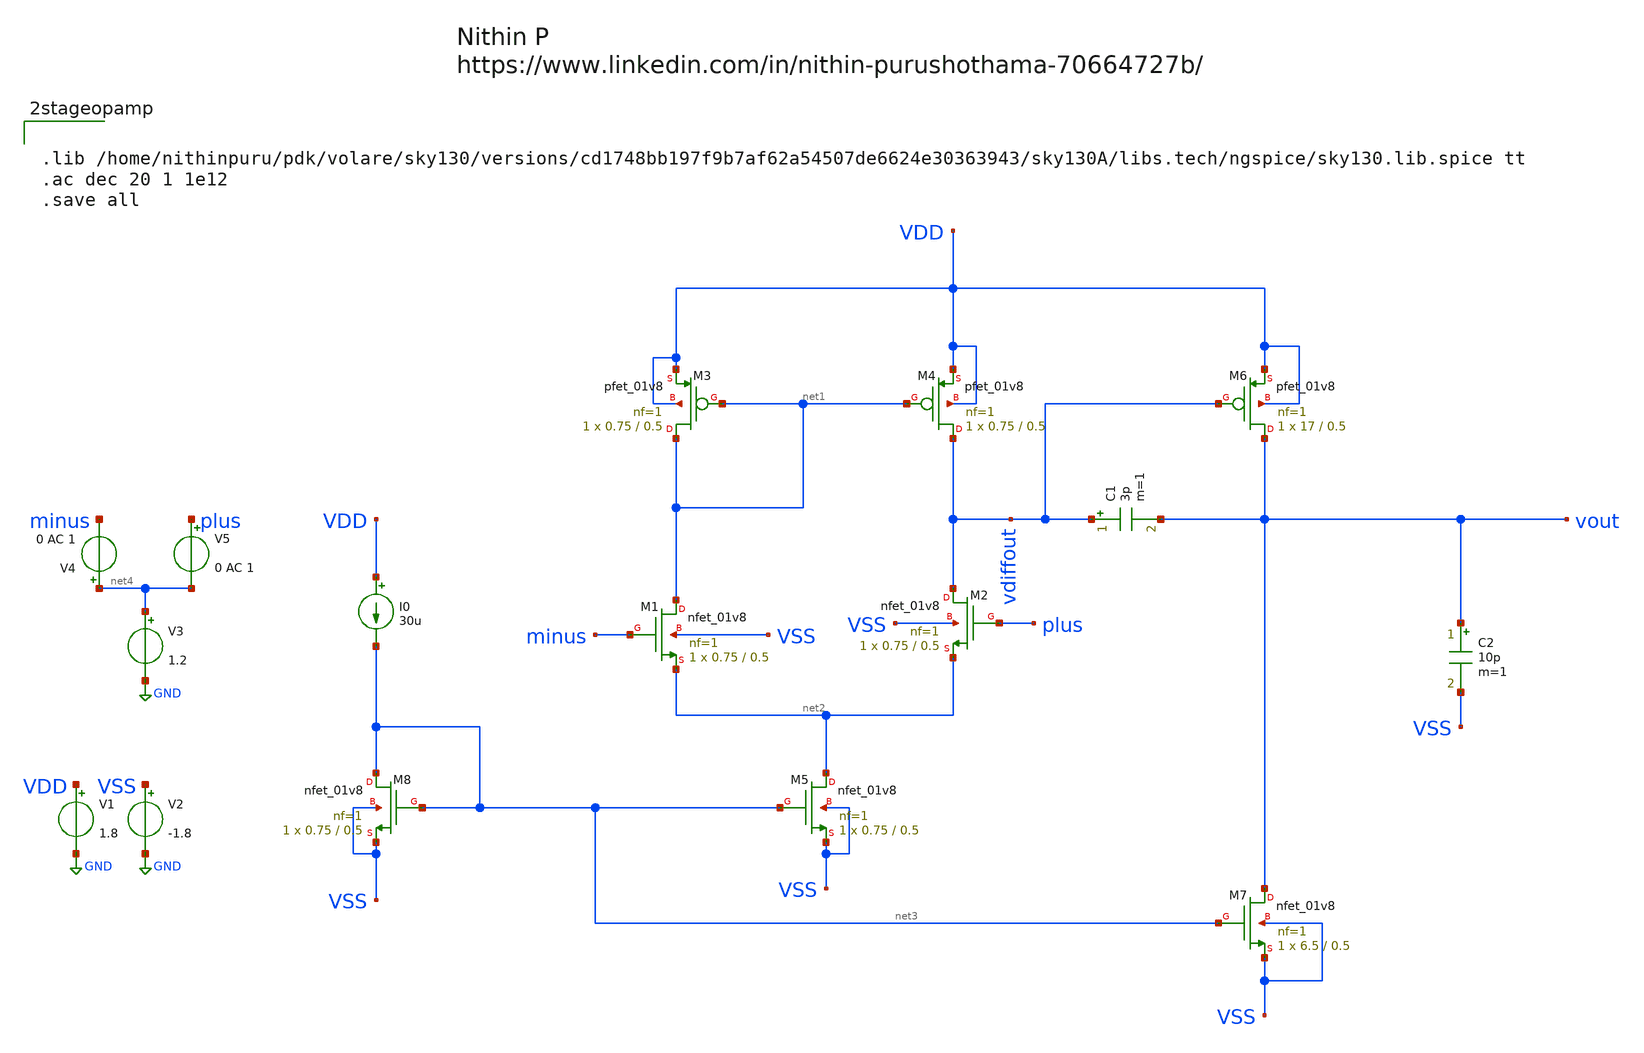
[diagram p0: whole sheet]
** sch_path: Schematics/Two stage Opamp Test bench/2stageopamptry.sch
**.subckt 2stageopamptry
XM1 net1 minus net2 VSS sky130_fd_pr__nfet_01v8 L=0.5 W=0.75 nf=1 ad='int((nf+1)/2) * W/nf * 0.29' as='int((nf+2)/2) * W/nf * 0.29'
+ pd='2*int((nf+1)/2) * (W/nf + 0.29)' ps='2*int((nf+2)/2) * (W/nf + 0.29)' nrd='0.29 / W' nrs='0.29 / W'
+ sa=0 sb=0 sd=0 mult=1 m=1
XM2 vdiffout plus net2 VSS sky130_fd_pr__nfet_01v8 L=0.5 W=0.75 nf=1 ad='int((nf+1)/2) * W/nf * 0.29'
+ as='int((nf+2)/2) * W/nf * 0.29' pd='2*int((nf+1)/2) * (W/nf + 0.29)' ps='2*int((nf+2)/2) * (W/nf + 0.29)'
+ nrd='0.29 / W' nrs='0.29 / W' sa=0 sb=0 sd=0 mult=1 m=1
XM5 net2 net3 VSS VSS sky130_fd_pr__nfet_01v8 L=0.5 W=0.75 nf=1 ad='int((nf+1)/2) * W/nf * 0.29' as='int((nf+2)/2) * W/nf * 0.29'
+ pd='2*int((nf+1)/2) * (W/nf + 0.29)' ps='2*int((nf+2)/2) * (W/nf + 0.29)' nrd='0.29 / W' nrs='0.29 / W'
+ sa=0 sb=0 sd=0 mult=1 m=1
XM8 net3 net3 VSS VSS sky130_fd_pr__nfet_01v8 L=0.5 W=0.75 nf=1 ad='int((nf+1)/2) * W/nf * 0.29' as='int((nf+2)/2) * W/nf * 0.29'
+ pd='2*int((nf+1)/2) * (W/nf + 0.29)' ps='2*int((nf+2)/2) * (W/nf + 0.29)' nrd='0.29 / W' nrs='0.29 / W'
+ sa=0 sb=0 sd=0 mult=1 m=1
XM7 vout net3 VSS VSS sky130_fd_pr__nfet_01v8 L=0.5 W=6.5 nf=1 ad='int((nf+1)/2) * W/nf * 0.29' as='int((nf+2)/2) * W/nf * 0.29'
+ pd='2*int((nf+1)/2) * (W/nf + 0.29)' ps='2*int((nf+2)/2) * (W/nf + 0.29)' nrd='0.29 / W' nrs='0.29 / W'
+ sa=0 sb=0 sd=0 mult=1 m=1
XM3 net1 net1 VDD VDD sky130_fd_pr__pfet_01v8 L=0.5 W=0.75 nf=1 ad='int((nf+1)/2) * W/nf * 0.29' as='int((nf+2)/2) * W/nf * 0.29'
+ pd='2*int((nf+1)/2) * (W/nf + 0.29)' ps='2*int((nf+2)/2) * (W/nf + 0.29)' nrd='0.29 / W' nrs='0.29 / W'
+ sa=0 sb=0 sd=0 mult=1 m=1
XM4 vdiffout net1 VDD VDD sky130_fd_pr__pfet_01v8 L=0.5 W=0.75 nf=1 ad='int((nf+1)/2) * W/nf * 0.29'
+ as='int((nf+2)/2) * W/nf * 0.29' pd='2*int((nf+1)/2) * (W/nf + 0.29)' ps='2*int((nf+2)/2) * (W/nf + 0.29)'
+ nrd='0.29 / W' nrs='0.29 / W' sa=0 sb=0 sd=0 mult=1 m=1
XM6 vout vdiffout VDD VDD sky130_fd_pr__pfet_01v8 L=0.5 W=17 nf=1 ad='int((nf+1)/2) * W/nf * 0.29' as='int((nf+2)/2) * W/nf * 0.29'
+ pd='2*int((nf+1)/2) * (W/nf + 0.29)' ps='2*int((nf+2)/2) * (W/nf + 0.29)' nrd='0.29 / W' nrs='0.29 / W'
+ sa=0 sb=0 sd=0 mult=1 m=1
I0 VDD net3 30u
C1 vdiffout vout 3p m=1
C2 vout VSS 10p m=1
V1 VDD GND 1.8
V2 VSS GND -1.8
V4 net4 minus 0 AC 1
V5 plus net4 0 AC 1
V3 net4 GND 1.2
**** begin user architecture code


.lib /home/nithinpuru/pdk/volare/sky130/versions/cd1748bb197f9b7af62a54507de6624e30363943/sky130A/libs.tech/ngspice/sky130.lib.spice tt
.ac dec 20 1 1e12
.save all

**** end user architecture code
**.ends
.GLOBAL GND
.end
